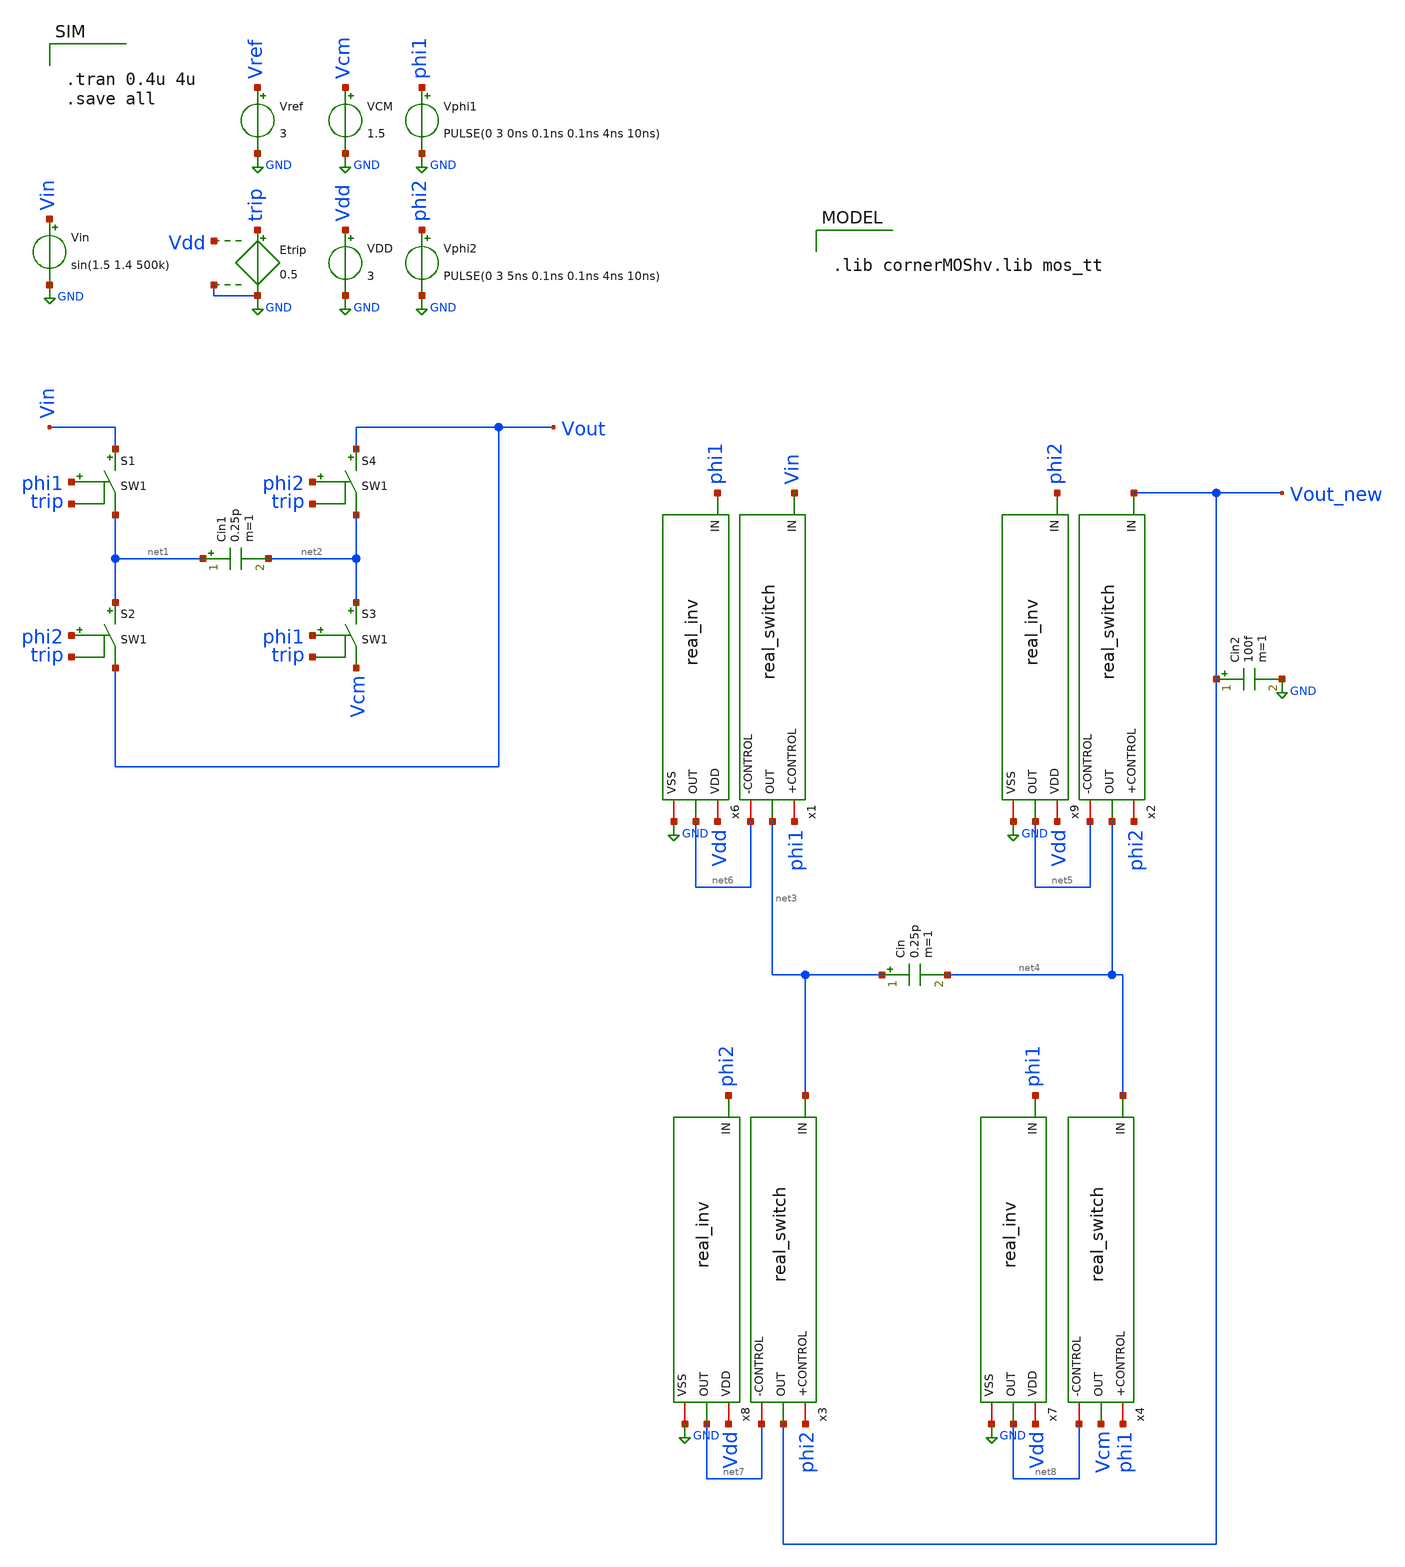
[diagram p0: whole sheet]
** sch_path: real_circuit/real_switches.sch
**.subckt real_switches
Etrip trip GND Vdd GND 0.5
Vref Vref GND 3
VDD Vdd GND 3
VCM Vcm GND 1.5
Vin Vin GND sin(1.5 1.4 500k)
Vphi1 phi1 GND PULSE(0 3 0ns 0.1ns 0.1ns 4ns 10ns)
Vphi2 phi2 GND PULSE(0 3 5ns 0.1ns 0.1ns 4ns 10ns)
S2 net1 Vout phi2 trip SW1
S1 Vin net1 phi1 trip SW1
S3 net2 Vcm phi1 trip SW1
S4 Vout net2 phi2 trip SW1
Cin net3 net4 0.25p m=1
x1 phi1 Vin net3 net6 real_switch
x2 phi2 Vout_new net4 net5 real_switch
x3 phi2 net3 Vout_new net7 real_switch
x4 phi1 net4 Vcm net8 real_switch
x6 Vdd phi1 net6 GND real_inv
x7 Vdd phi1 net8 GND real_inv
x8 Vdd phi2 net7 GND real_inv
x9 Vdd phi2 net5 GND real_inv
Cin1 net1 net2 0.25p m=1
Cin2 Vout_new GND 100f m=1
**** begin user architecture code


.tran 0.4u 4u
.save all



.lib cornerMOShv.lib mos_tt

**** end user architecture code
**.ends

* expanding   symbol:  /foss/designs/delta_sigma/real/real_switch.sym # of pins=4
** sym_path: real_circuit/real_switch.sym
** sch_path: real_circuit/real_switch.sch
.subckt real_switch +CONTROL IN OUT -CONTROL
*.ipin IN
*.opin OUT
*.iopin +CONTROL
*.iopin -CONTROL
XM1 OUT -CONTROL IN IN sg13_hv_pmos w=3u l=0.4u ng=1 m=1 mm_ok=1
XM2 OUT +CONTROL IN IN sg13_hv_nmos w=1u l=0.45u ng=1 m=1 mm_ok=1
.ends


* expanding   symbol:  /foss/designs/delta_sigma/real/real_inv.sym # of pins=4
** sym_path: real_circuit/real_inv.sym
** sch_path: real_circuit/real_inv.sch
.subckt real_inv VDD IN OUT VSS
*.iopin VDD
*.iopin VSS
*.ipin IN
*.opin OUT
XM1 OUT IN VDD VDD sg13_hv_pmos w=0.6u l=0.4u ng=1 m=1 mm_ok=1
XM2 OUT IN VSS VSS sg13_hv_nmos w=0.3u l=0.45u ng=1 m=1 mm_ok=1
.ends

.GLOBAL GND
**** begin user architecture code
.MODEL SW1 SW   VT=0.9 VH=0.01  RON=0.1 ROFF=10G
**** end user architecture code
.end
